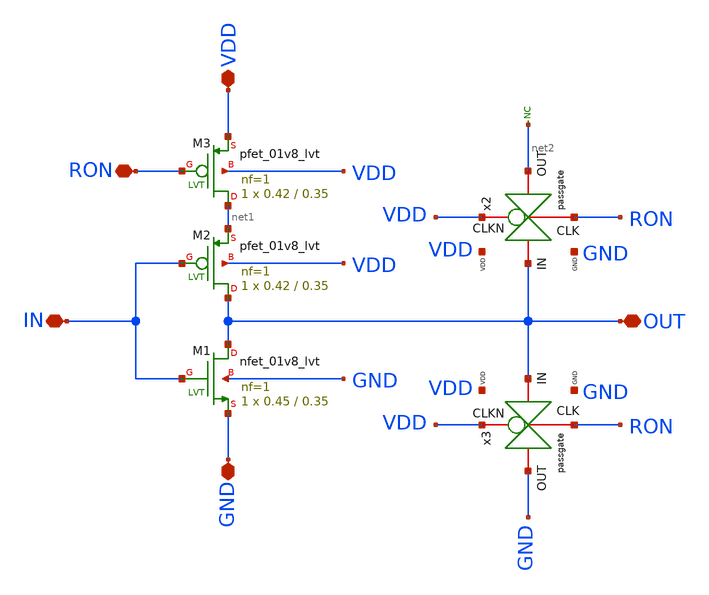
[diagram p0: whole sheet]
** sch_path: LVT/rovcel4_LVT/rovcel4_LVT.sch
**.subckt rovcel4_LVT OUT RON IN GND VDD
*.iopin OUT
*.iopin RON
*.iopin IN
*.iopin GND
*.iopin VDD
XM1 OUT IN GND GND sky130_fd_pr__nfet_01v8_lvt L=0.35 W=0.45 nf=1 ad='int((nf+1)/2) * W/nf * 0.29' as='int((nf+2)/2) * W/nf * 0.29'
+ pd='2*int((nf+1)/2) * (W/nf + 0.29)' ps='2*int((nf+2)/2) * (W/nf + 0.29)' nrd='0.29 / W' nrs='0.29 / W'
+ sa=0 sb=0 sd=0 mult=1 m=1
XM2 OUT IN net1 VDD sky130_fd_pr__pfet_01v8_lvt L=0.35 W=0.42 nf=1 ad='int((nf+1)/2) * W/nf * 0.29' as='int((nf+2)/2) * W/nf * 0.29'
+ pd='2*int((nf+1)/2) * (W/nf + 0.29)' ps='2*int((nf+2)/2) * (W/nf + 0.29)' nrd='0.29 / W' nrs='0.29 / W'
+ sa=0 sb=0 sd=0 mult=1 m=1
XM3 net1 RON VDD VDD sky130_fd_pr__pfet_01v8_lvt L=0.35 W=0.42 nf=1 ad='int((nf+1)/2) * W/nf * 0.29'
+ as='int((nf+2)/2) * W/nf * 0.29' pd='2*int((nf+1)/2) * (W/nf + 0.29)' ps='2*int((nf+2)/2) * (W/nf + 0.29)'
+ nrd='0.29 / W' nrs='0.29 / W' sa=0 sb=0 sd=0 mult=1 m=1
* noconn #net2
x2 VDD OUT net2 RON GND VDD passgate
x3 VDD OUT GND RON GND VDD passgate
**.ends
.end
